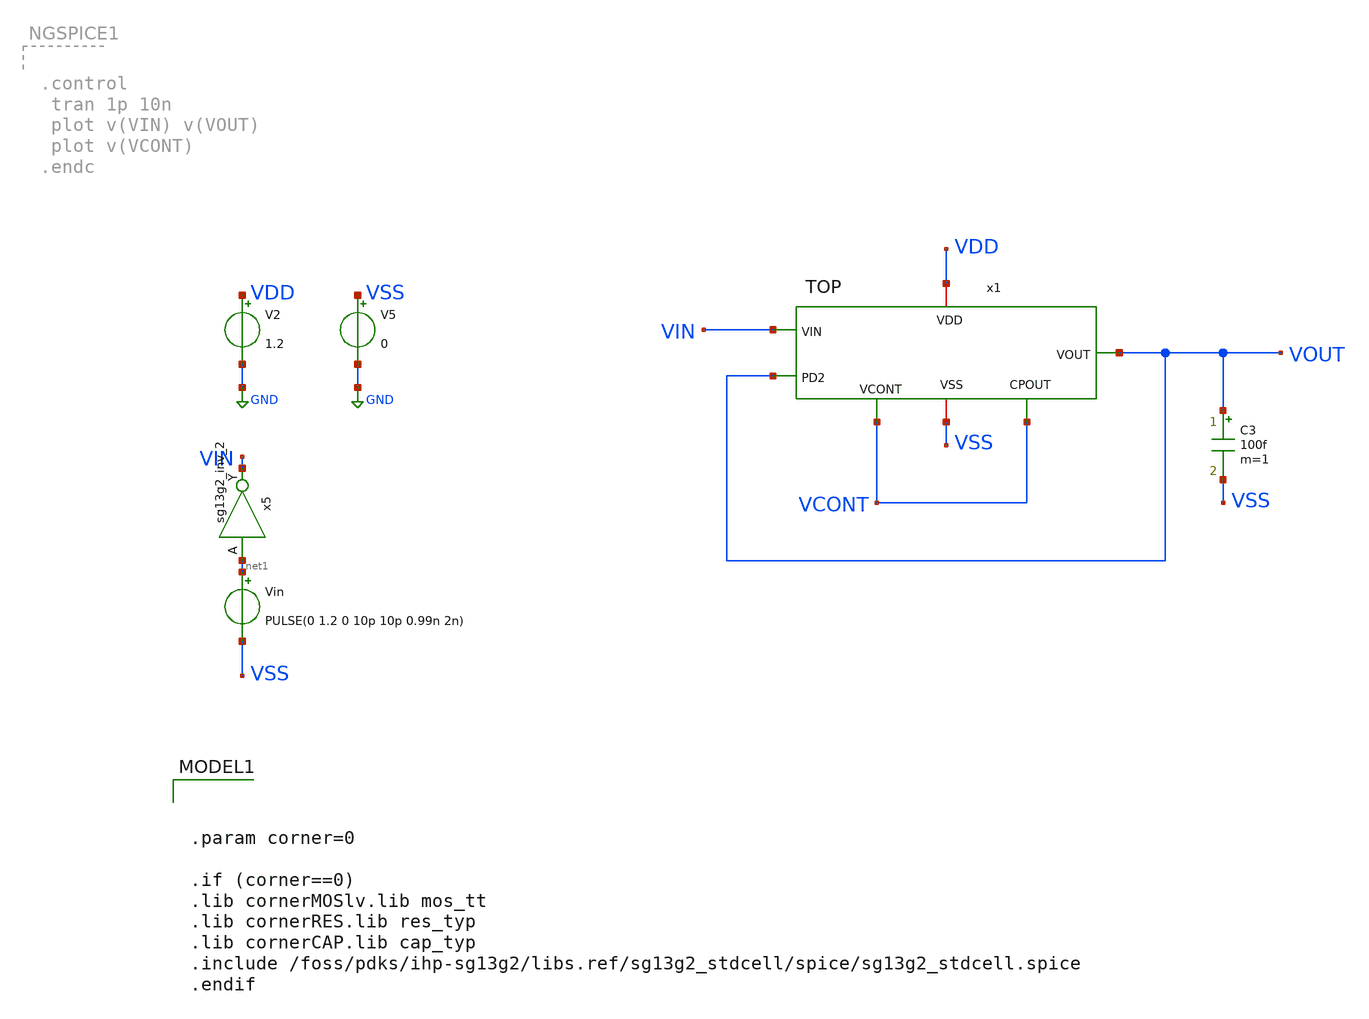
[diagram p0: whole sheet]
** sch_path: testbenchs/tb_TOP2.sch
**.subckt tb_TOP2
Vin net1 VSS PULSE(0 1.2 0 10p 10p 0.99n 2n)
C3 VOUT VSS 100f m=1
V2 VDD GND 1.2
V5 VSS GND 0
x5 VIN net1 VDD VSS sg13g2_inv_2
x1 VDD VOUT VIN VCONT VSS VCONT VOUT TOP
**** begin user architecture code


.param corner=0

.if (corner==0)
.lib cornerMOSlv.lib mos_tt
.lib cornerRES.lib res_typ
.lib cornerCAP.lib cap_typ
.include /foss/pdks/ihp-sg13g2/libs.ref/sg13g2_stdcell/spice/sg13g2_stdcell.spice
.endif



.control
* ---- settings you tweak ----


   * ---- user settings ----
  let vlow  = 0
  let vhigh = 1.2
  let v50   = vlow + 0.5*(vhigh - vlow)

  let start_edge = 0     ; skip early edges (settling)
  let N = 200             ; number of phase samples



  tran 1p 10n

  * ---- allocate vectors ----
  let tvec   = vector(N)
  let phivec = vector(N)

  let k = 0
  let i = start_edge

  while k < N
    * crossing times
    meas tran tin      WHEN v(VIN)=v50  RISE=i
    meas tran tout     WHEN v(VOUT)=v50 RISE=i
    meas tran tin_next WHEN v(VIN)=v50  RISE=(i+1)

    * delay + period
    let dt = tout - tin
    let T  = tin_next - tin

    * phase in degrees (per-cycle)
    let phi = 360*dt/T
    let phi = phi - 360*floor(phi/360)

    * store sample at time = tin
    let tvec[k]   = tin
    let phivec[k] = phi

    let k = k + 1
    let i = i + 1
  end

  * plot phase vs time (one point per cycle)
  plot phivec vs tvec
  *plot v(VCONT)
  plot v(VIN) v(VOUT)
.endc


**** end user architecture code
**.ends
.GLOBAL GND
.end
